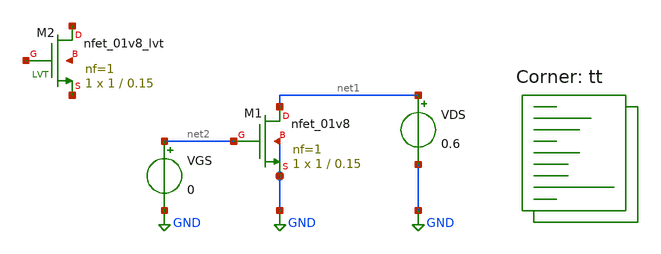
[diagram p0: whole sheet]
** sch_path: pll/lc_vco_lib/Ahmed_Elshahat/CMOS_LC_VCO/NMOS_charts/spice_files/NMOS_char.sch
**.subckt NMOS_char
XM1 net1 net2 GND GND sky130_fd_pr__nfet_01v8 L=0.15 W=1 nf=1 ad='int((1 + 1)/2) * 1 / 1 * 0.29' as='int((1 + 2)/2) * 1 / 1 * 0.29'
+ pd='2*int((1 + 1)/2) * (1 / 1 + 0.29)' ps='2*int((1 + 2)/2) * (1 / 1 + 0.29)' nrd='0.29 / 1 ' nrs='0.29 / 1 '
+ sa=0 sb=0 sd=0 mult=1 m=1
VDS net1 GND 0.6
VGS net2 GND 0
XM2 net3 net4 net5 net6 sky130_fd_pr__nfet_01v8_lvt L=0.15 W=1 nf=1 ad='int((1 + 1)/2) * 1 / 1 * 0.29'
+ as='int((1 + 2)/2) * 1 / 1 * 0.29' pd='2*int((1 + 1)/2) * (1 / 1 + 0.29)' ps='2*int((1 + 2)/2) * (1 / 1 + 0.29)'
+ nrd='0.29 / 1 ' nrs='0.29 / 1 ' sa=0 sb=0 sd=0 mult=1 m=1
**** begin user architecture code
.lib $::SKYWATER_MODELS/sky130.lib.spice tt
**** end user architecture code
**.ends
.GLOBAL GND
.end
